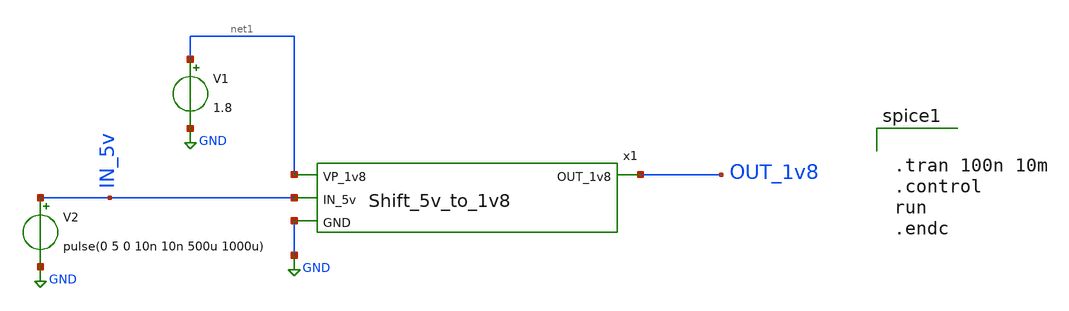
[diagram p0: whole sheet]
** sch_path: ADC/16bit_C2C/MagicAndSpice/EE431_FinalProj/shift_down_tb.sch
**.subckt shift_down_tb
x1 net1 OUT_1v8 IN_5v GND Shift_5v_to_1v8
V1 net1 GND 1.8
V2 IN_5v GND pulse(0 5 0 10n 10n 500u 1000u)
**** begin user architecture code
 .lib $::SKYWATER_MODELS/sky130.lib.spice tt


.tran 100n 10m
.control
run
.endc

**** end user architecture code
**.ends
.GLOBAL GND
.end
